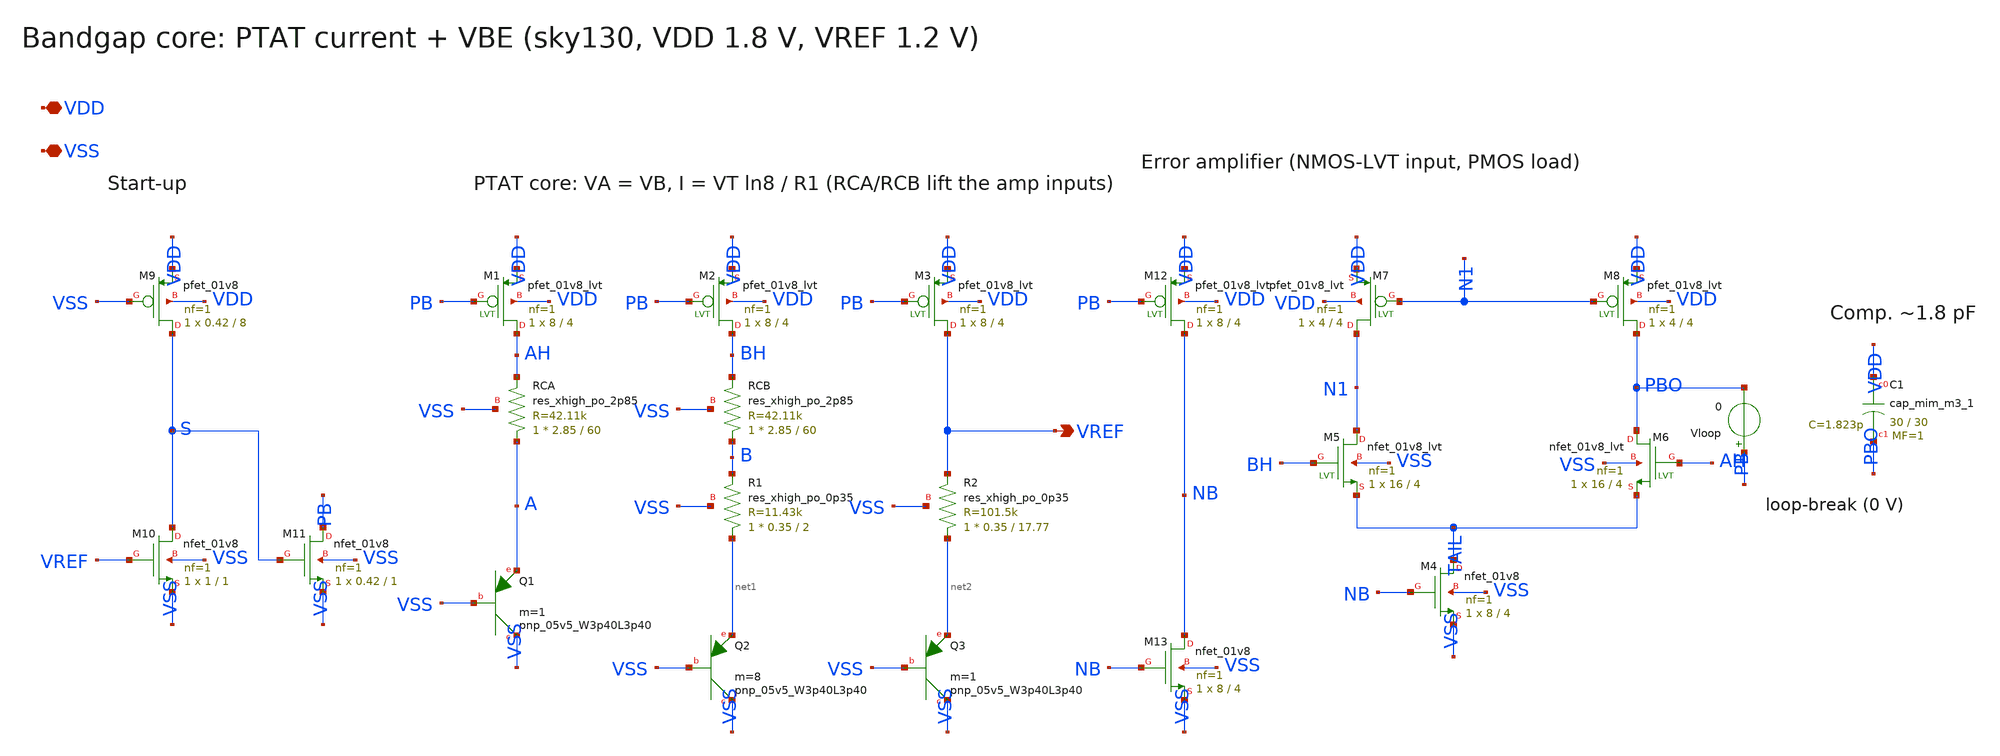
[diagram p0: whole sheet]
** sch_path: xschem/bandgap_core.sch
**.subckt bandgap_core VREF VDD VSS
*.opin VREF
*.iopin VDD
*.iopin VSS
XM9 S VSS VDD VDD sky130_fd_pr__pfet_01v8 L=8 W=0.42 nf=1 ad=0.1218 as=0.1218 pd=1.42 ps=1.42
+ nrd=0.6905 nrs=0.6905 sa=0 sb=0 sd=0 mult=1 m=1
XM10 S VREF VSS VSS sky130_fd_pr__nfet_01v8 L=1 W=1 nf=1 ad=0.29 as=0.29 pd=2.58 ps=2.58 nrd=0.29
+ nrs=0.29 sa=0 sb=0 sd=0 mult=1 m=1
XM11 PB S VSS VSS sky130_fd_pr__nfet_01v8 L=1 W=0.42 nf=1 ad=0.1218 as=0.1218 pd=1.42 ps=1.42
+ nrd=0.6905 nrs=0.6905 sa=0 sb=0 sd=0 mult=1 m=1
XM1 AH PB VDD VDD sky130_fd_pr__pfet_01v8_lvt L=4 W=8 nf=1 ad=2.32 as=2.32 pd=16.58 ps=16.58
+ nrd=0.0362 nrs=0.0362 sa=0 sb=0 sd=0 mult=1 m=1
XM2 BH PB VDD VDD sky130_fd_pr__pfet_01v8_lvt L=4 W=8 nf=1 ad=2.32 as=2.32 pd=16.58 ps=16.58
+ nrd=0.0362 nrs=0.0362 sa=0 sb=0 sd=0 mult=1 m=1
XM3 VREF PB VDD VDD sky130_fd_pr__pfet_01v8_lvt L=4 W=8 nf=1 ad=2.32 as=2.32 pd=16.58 ps=16.58
+ nrd=0.0362 nrs=0.0362 sa=0 sb=0 sd=0 mult=1 m=1
XQ1 VSS VSS A sky130_fd_pr__pnp_05v5_W3p40L3p40 m=1
XRCA A AH VSS sky130_fd_pr__res_xhigh_po_2p85 L=60 mult=1 m=1
XR1 net1 B VSS sky130_fd_pr__res_xhigh_po_0p35 L=2 mult=1 m=1
XQ2 VSS VSS net1 sky130_fd_pr__pnp_05v5_W3p40L3p40 m=8
XRCB B BH VSS sky130_fd_pr__res_xhigh_po_2p85 L=60 mult=1 m=1
XR2 net2 VREF VSS sky130_fd_pr__res_xhigh_po_0p35 L=17.77 mult=1 m=1
XQ3 VSS VSS net2 sky130_fd_pr__pnp_05v5_W3p40L3p40 m=1
XM12 NB PB VDD VDD sky130_fd_pr__pfet_01v8_lvt L=4 W=8 nf=1 ad=2.32 as=2.32 pd=16.58 ps=16.58
+ nrd=0.0362 nrs=0.0362 sa=0 sb=0 sd=0 mult=1 m=1
XM13 NB NB VSS VSS sky130_fd_pr__nfet_01v8 L=4 W=8 nf=1 ad=2.32 as=2.32 pd=16.58 ps=16.58 nrd=0.0362
+ nrs=0.0362 sa=0 sb=0 sd=0 mult=1 m=1
XM7 N1 N1 VDD VDD sky130_fd_pr__pfet_01v8_lvt L=4 W=4 nf=1 ad=1.16 as=1.16 pd=8.58 ps=8.58
+ nrd=0.0725 nrs=0.0725 sa=0 sb=0 sd=0 mult=1 m=1
XM8 PBO N1 VDD VDD sky130_fd_pr__pfet_01v8_lvt L=4 W=4 nf=1 ad=1.16 as=1.16 pd=8.58 ps=8.58
+ nrd=0.0725 nrs=0.0725 sa=0 sb=0 sd=0 mult=1 m=1
XM5 N1 BH TAIL VSS sky130_fd_pr__nfet_01v8_lvt L=4 W=16 nf=1 ad=4.64 as=4.64 pd=32.58 ps=32.58
+ nrd=0.0181 nrs=0.0181 sa=0 sb=0 sd=0 mult=1 m=1
XM6 PBO AH TAIL VSS sky130_fd_pr__nfet_01v8_lvt L=4 W=16 nf=1 ad=4.64 as=4.64 pd=32.58 ps=32.58
+ nrd=0.0181 nrs=0.0181 sa=0 sb=0 sd=0 mult=1 m=1
XM4 TAIL NB VSS VSS sky130_fd_pr__nfet_01v8 L=4 W=8 nf=1 ad=2.32 as=2.32 pd=16.58 ps=16.58
+ nrd=0.0362 nrs=0.0362 sa=0 sb=0 sd=0 mult=1 m=1
Vloop PB PBO 0
XC1 VDD PBO sky130_fd_pr__cap_mim_m3_1 W=30 L=30 MF=1 m=1
**.ends
.end
